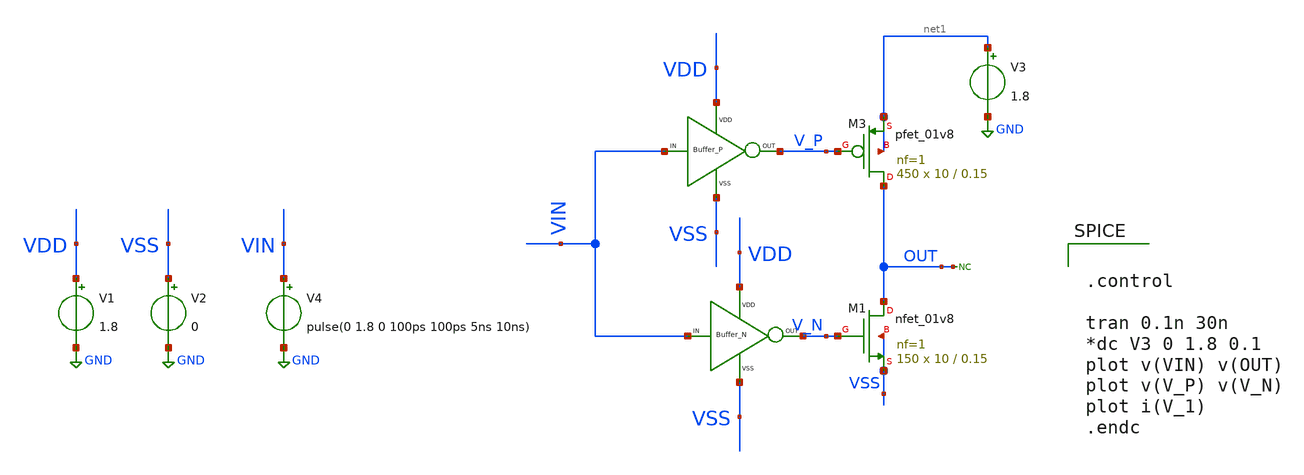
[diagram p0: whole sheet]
** sch_path: xschem/DC_DC_Converter_xschem/OTHERS/DC_DC_Converter_JV10/BUFFER/top_final.sch
**.subckt top_final
XM3 OUT V_P net1 net1 sky130_fd_pr__pfet_01v8 L=0.15 W=10 nf=1 ad='int((nf+1)/2) * W/nf * 0.29' as='int((nf+2)/2) * W/nf * 0.29'
+ pd='2*int((nf+1)/2) * (W/nf + 0.29)' ps='2*int((nf+2)/2) * (W/nf + 0.29)' nrd='0.29 / W' nrs='0.29 / W'
+ sa=0 sb=0 sd=0 mult=450 m=450
XM1 OUT V_N VSS VSS sky130_fd_pr__nfet_01v8 L=0.15 W=10 nf=1 ad='int((nf+1)/2) * W/nf * 0.29' as='int((nf+2)/2) * W/nf * 0.29'
+ pd='2*int((nf+1)/2) * (W/nf + 0.29)' ps='2*int((nf+2)/2) * (W/nf + 0.29)' nrd='0.29 / W' nrs='0.29 / W'
+ sa=0 sb=0 sd=0 mult=150 m=150
V1 VDD GND 1.8
V2 VSS GND 0
* noconn OUT
V4 VIN GND pulse(0 1.8 0 100ps 100ps 5ns 10ns)
X1 VIN V_N VDD VSS BUFFER_N
X2 VIN V_P VDD VSS BUFFER_P
V3 net1 GND 1.8
**** begin user architecture code

** opencircuitdesign pdks install
.lib $::SKYWATER_MODELS/sky130.lib.spice tt




.control

tran 0.1n 30n
*dc V3 0 1.8 0.1
plot v(VIN) v(OUT)
plot v(V_P) v(V_N)
plot i(V_1)
.endc


**** end user architecture code
**.ends
.GLOBAL GND
.end
